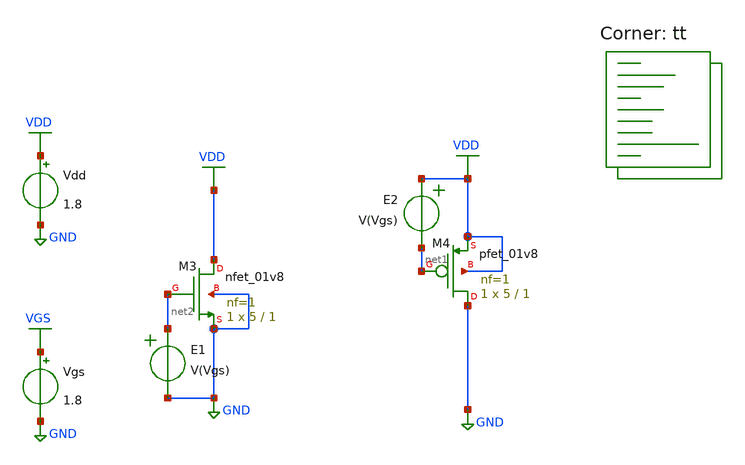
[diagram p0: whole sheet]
** sch_path: characterization.sch
**.subckt characterization
Vgs VGS GND 1.8
Vdd VDD GND 1.8
XM3 VDD net2 GND GND sky130_fd_pr__nfet_01v8 L=1 W=5 nf=1 ad='int((nf+1)/2) * W/nf * 0.29' as='int((nf+2)/2) * W/nf * 0.29'
+ pd='2*int((nf+1)/2) * (W/nf + 0.29)' ps='2*int((nf+2)/2) * (W/nf + 0.29)' nrd='0.29 / W' nrs='0.29 / W'
+ sa=0 sb=0 sd=0 mult=1 m=1
XM4 GND net1 VDD VDD sky130_fd_pr__pfet_01v8 L=1 W=5 nf=1 ad='int((nf+1)/2) * W/nf * 0.29' as='int((nf+2)/2) * W/nf * 0.29'
+ pd='2*int((nf+1)/2) * (W/nf + 0.29)' ps='2*int((nf+2)/2) * (W/nf + 0.29)' nrd='0.29 / W' nrs='0.29 / W'
+ sa=0 sb=0 sd=0 mult=1 m=1
E1 net2 GND VOL=' V(Vgs) '
E2 VDD net1 VOL=' V(Vgs) '
**** begin user architecture code



.options savecurrents

.control
save all
dc vgs 0 1.8 0.01 vdd 0 1.8 0.2
let id_nmos=@m.xm3.msky130_fd_pr__nfet_01v8[id]
let id_pmos=@m.xm4.msky130_fd_pr__pfet_01v8[id]


print v(vthn) v(vthp)
plot id_nmos id_pmos title 'V_GS characteristic' xlabel 'V_GS' ylabel 'Current'
write characterization.raw

set appendwrite
.endc


.lib $::SKYWATER_MODELS/sky130.lib.spice tt
**** end user architecture code
**.ends
.GLOBAL GND
.GLOBAL VGS
.GLOBAL VDD
.end
